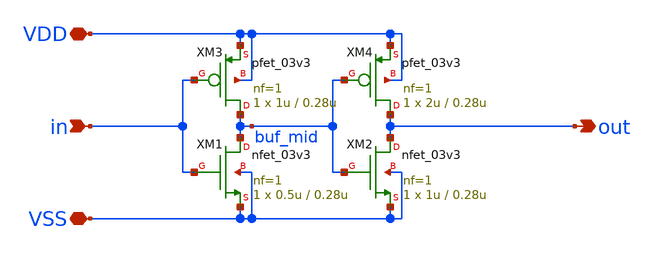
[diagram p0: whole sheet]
** sch_path: adc_sar_comp_buffer.sch
**.subckt adc_sar_comp_buffer VDD VSS in out
*.iopin VDD
*.iopin VSS
*.ipin in
*.opin out
XM1 buf_mid in VSS VSS nfet_03v3 L=0.28u W=0.5u nf=1 ad='int((nf+1)/2) * W/nf * 0.18u' as='int((nf+2)/2) * W/nf * 0.18u'
+ pd='2*int((nf+1)/2) * (W/nf + 0.18u)' ps='2*int((nf+2)/2) * (W/nf + 0.18u)' nrd='0.18u / W' nrs='0.18u / W'
+ sa=0 sb=0 sd=0 m=1
XM2 out buf_mid VSS VSS nfet_03v3 L=0.28u W=1u nf=1 ad='int((nf+1)/2) * W/nf * 0.18u' as='int((nf+2)/2) * W/nf * 0.18u'
+ pd='2*int((nf+1)/2) * (W/nf + 0.18u)' ps='2*int((nf+2)/2) * (W/nf + 0.18u)' nrd='0.18u / W' nrs='0.18u / W'
+ sa=0 sb=0 sd=0 m=1
XM3 buf_mid in VDD VDD pfet_03v3 L=0.28u W=1u nf=1 ad='int((nf+1)/2) * W/nf * 0.18u' as='int((nf+2)/2) * W/nf * 0.18u'
+ pd='2*int((nf+1)/2) * (W/nf + 0.18u)' ps='2*int((nf+2)/2) * (W/nf + 0.18u)' nrd='0.18u / W' nrs='0.18u / W'
+ sa=0 sb=0 sd=0 m=1
XM4 out buf_mid VDD VDD pfet_03v3 L=0.28u W=2u nf=1 ad='int((nf+1)/2) * W/nf * 0.18u' as='int((nf+2)/2) * W/nf * 0.18u'
+ pd='2*int((nf+1)/2) * (W/nf + 0.18u)' ps='2*int((nf+2)/2) * (W/nf + 0.18u)' nrd='0.18u / W' nrs='0.18u / W'
+ sa=0 sb=0 sd=0 m=1
**.ends
.end
